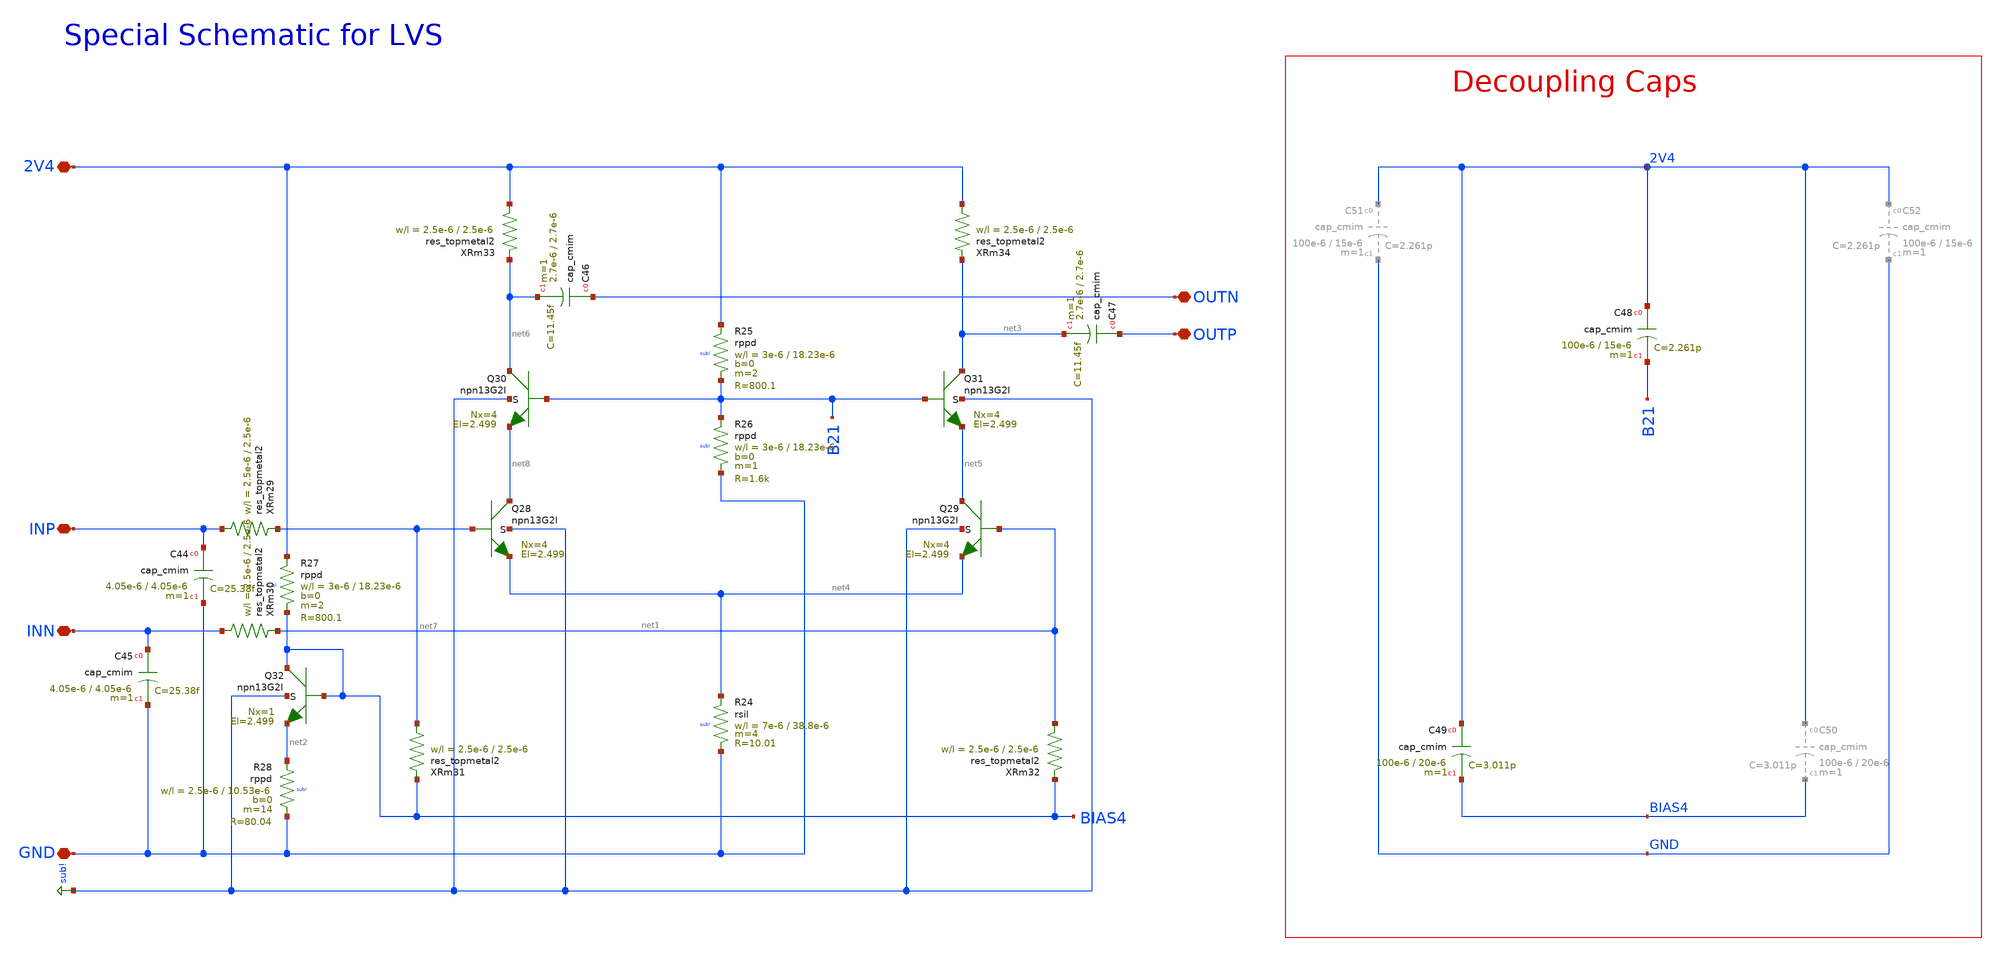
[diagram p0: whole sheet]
** sch_path: mWATTBAT/design_data/lvs/TXAMP_150GD_LVS.sch
**.subckt TXAMP_150GD_LVS 2V4 GND OUTN OUTP INP INN
*.iopin 2V4
*.iopin GND
*.iopin OUTN
*.iopin OUTP
*.iopin INP
*.iopin INN
XQ28 net8 net7 net4 sub! npn13G2l Nx=4 El=2.499 mm_ok=1
XQ29 net5 net1 net4 sub! npn13G2l Nx=4 El=2.499 mm_ok=1
XQ32 BIAS4 BIAS4 net2 sub! npn13G2l Nx=1 El=2.499 mm_ok=1
XQ30 net6 B21 net8 sub! npn13G2l Nx=4 El=2.499 mm_ok=1
XQ31 net3 B21 net5 sub! npn13G2l Nx=4 El=2.499 mm_ok=1
XR27 2V4 BIAS4 sub! rppd w=3e-6 l=18.23e-6 m=2 b=0 mm_ok=1
XC44 INP GND cap_cmim w=4.05e-6 l=4.05e-6 m=1 mm_ok=1
XC45 INN GND cap_cmim w=4.05e-6 l=4.05e-6 m=1 mm_ok=1
XC46 OUTN net6 cap_cmim w=2.7e-6 l=2.7e-6 m=1 mm_ok=1
XC47 OUTP net3 cap_cmim w=2.7e-6 l=2.7e-6 m=1 mm_ok=1
XR28 net2 GND sub! rppd w=2.5e-6 l=10.53e-6 m=14 b=0 mm_ok=1
XR25 2V4 B21 sub! rppd w=3e-6 l=18.23e-6 m=2 b=0 mm_ok=1
XR26 B21 GND sub! rppd w=3e-6 l=18.23e-6 m=1 b=0 mm_ok=1
XC49 2V4 BIAS4 cap_cmim w=100e-6 l=20e-6 m=1 mm_ok=1
XC48 2V4 B21 cap_cmim w=100e-6 l=15e-6 m=1 mm_ok=1
XR24 net4 GND sub! rsil w=7e-6 l=38.8e-6 m=4 mm_ok=1
XRm29 INP net7 res_topmetal2 w=2.5e-6 l=2.5e-6
XRm30 INN net1 res_topmetal2 w=2.5e-6 l=2.5e-6
XRm31 net7 BIAS4 res_topmetal2 w=2.5e-6 l=2.5e-6
XRm32 net1 BIAS4 res_topmetal2 w=2.5e-6 l=2.5e-6
XRm33 2V4 net6 res_topmetal2 w=2.5e-6 l=2.5e-6
XRm34 2V4 net3 res_topmetal2 w=2.5e-6 l=2.5e-6
**.ends
.GLOBAL sub!
.end
